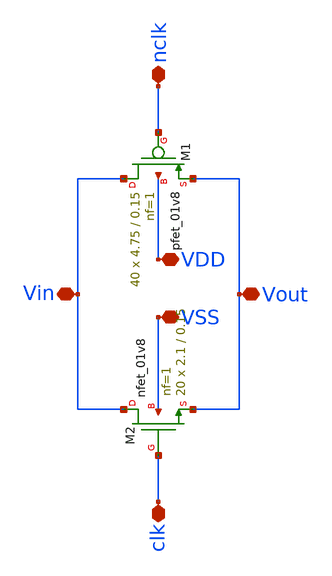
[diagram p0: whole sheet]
** sch_path: TT/tgate_force10.sch
**.subckt tgate_force10 nclk clk VDD VSS Vout Vin
*.iopin nclk
*.iopin clk
*.iopin VDD
*.iopin VSS
*.iopin Vout
*.iopin Vin
XM1 Vin nclk Vout VDD sky130_fd_pr__pfet_01v8 L=0.15 W=4.75 nf=1 ad='int((nf+1)/2) * W/nf * 0.29' as='int((nf+2)/2) * W/nf * 0.29'
+ pd='2*int((nf+1)/2) * (W/nf + 0.29)' ps='2*int((nf+2)/2) * (W/nf + 0.29)' nrd='0.29 / W' nrs='0.29 / W'
+ sa=0 sb=0 sd=0 mult=40 m=40
XM2 Vin clk Vout VSS sky130_fd_pr__nfet_01v8 L=0.15 W=2.1 nf=1 ad='int((nf+1)/2) * W/nf * 0.29' as='int((nf+2)/2) * W/nf * 0.29'
+ pd='2*int((nf+1)/2) * (W/nf + 0.29)' ps='2*int((nf+2)/2) * (W/nf + 0.29)' nrd='0.29 / W' nrs='0.29 / W'
+ sa=0 sb=0 sd=0 mult=20 m=20
**.ends
.end
